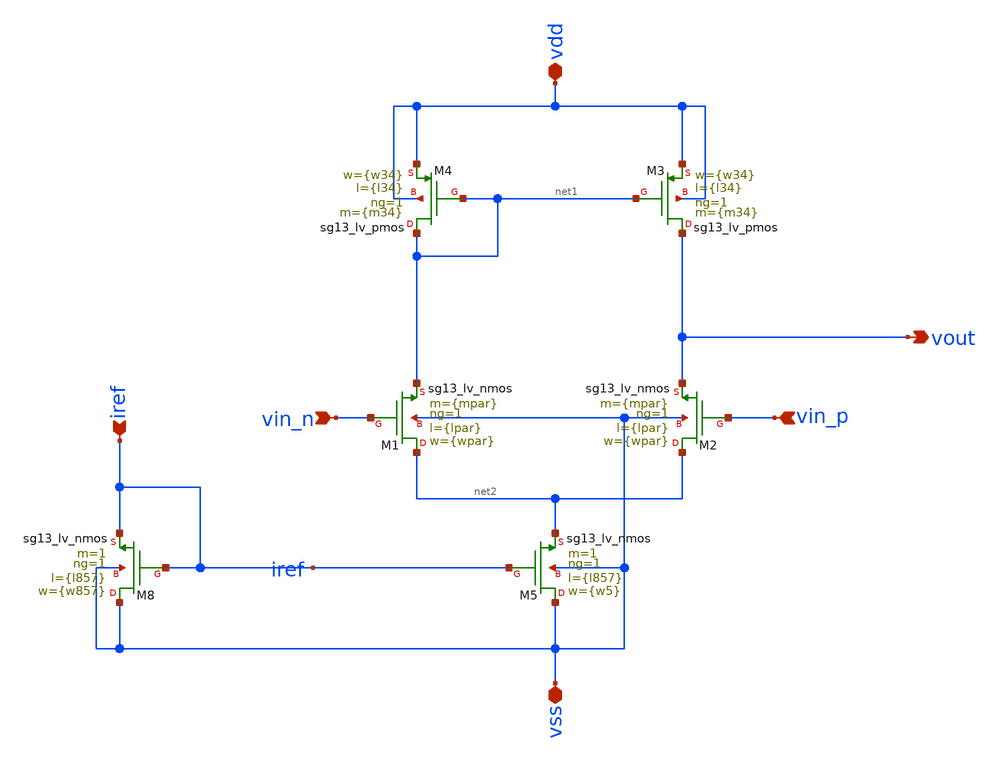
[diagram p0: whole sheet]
** sch_path: ihp_ota_v2.sch
**.subckt ihp_ota_v2 iref vin_n vin_p vdd vss vout
*.ipin iref
*.ipin vin_n
*.ipin vin_p
*.iopin vdd
*.iopin vss
*.opin vout
XM1 net2 vin_n net1 vss sg13_lv_nmos w={wpar} l={lpar} ng=1 m={mpar} mm_ok=1
XM2 net2 vin_p vout vss sg13_lv_nmos w={wpar} l={lpar} ng=1 m={mpar} mm_ok=1
XM3 vout net1 vdd vdd sg13_lv_pmos w={w34} l={l34} ng=1 m={m34} mm_ok=1
XM4 net1 net1 vdd vdd sg13_lv_pmos w={w34} l={l34} ng=1 m={m34} mm_ok=1
XM5 vss iref net2 vss sg13_lv_nmos w={w5} l={l857} ng=1 m=1 mm_ok=1
XM8 vss iref iref vss sg13_lv_nmos w={w857} l={l857} ng=1 m=1 mm_ok=1
**.ends
.end
